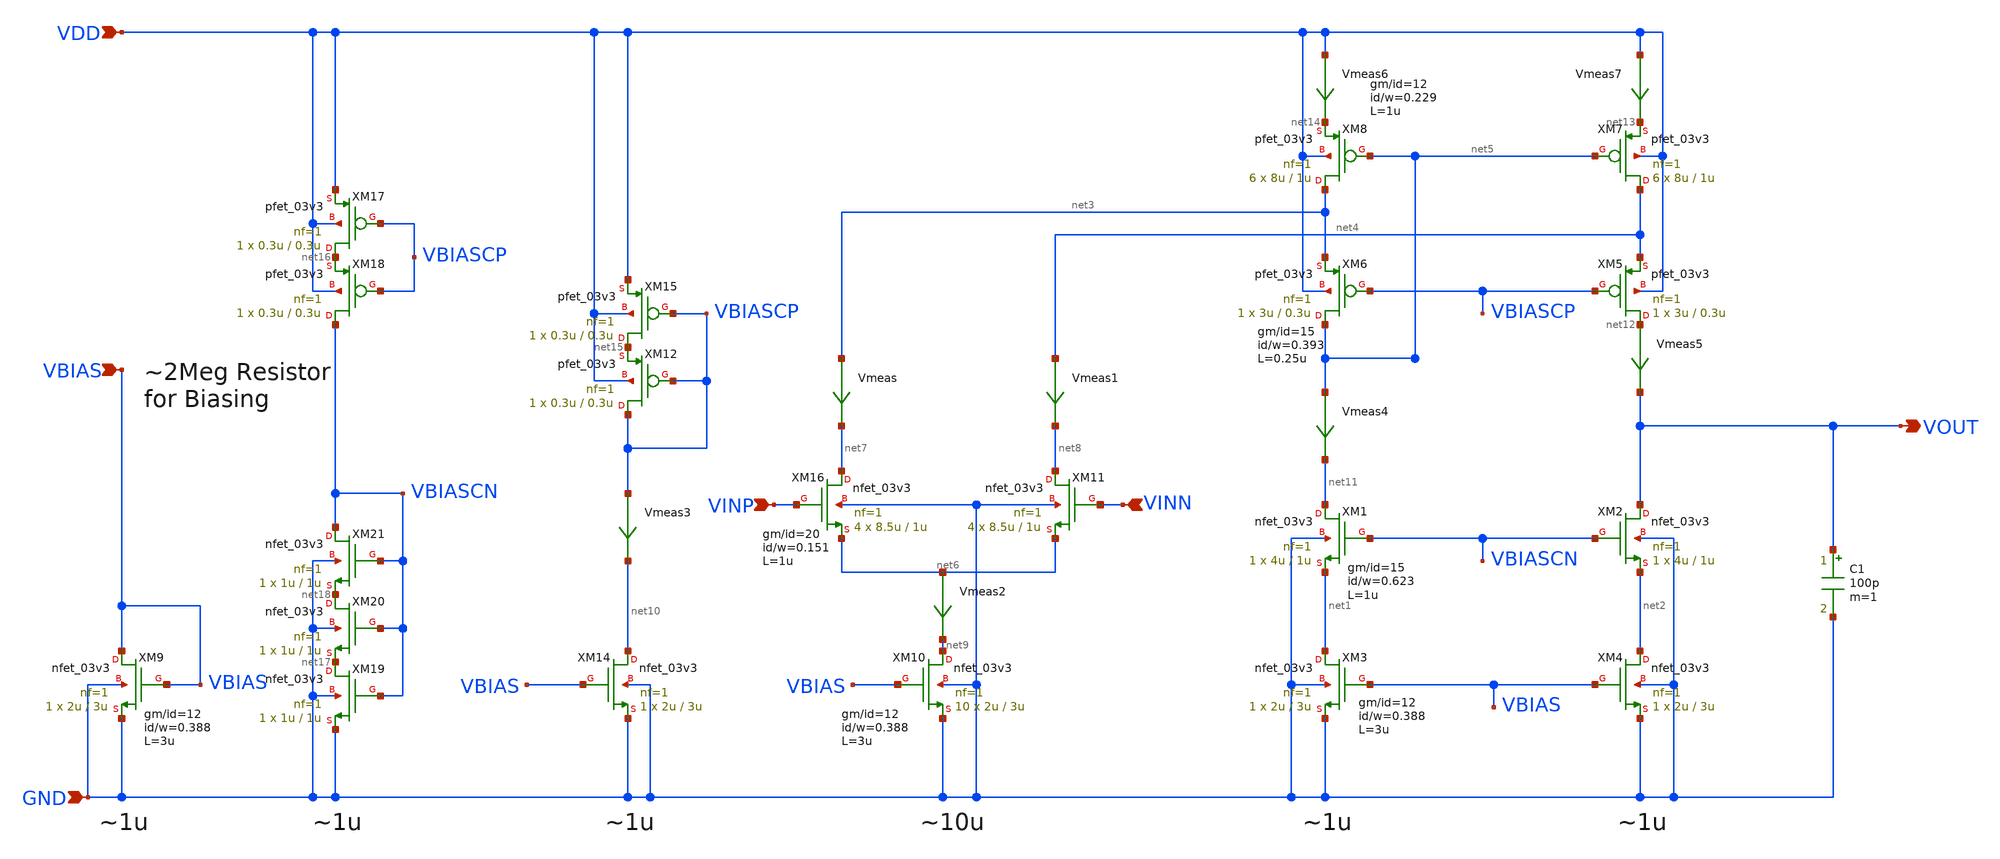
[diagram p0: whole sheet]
** sch_path: SCH/XSCHEM/TTGF0P3_LPCAS_FC_OTA.sch
**.subckt TTGF0P3_LPCAS_FC_OTA VOUT VINP VINN VDD VBIAS GND
*.opin VOUT
*.ipin VINP
*.ipin VINN
*.ipin VDD
*.ipin VBIAS
*.ipin GND
XM1 net11 VBIASCN net1 GND nfet_03v3 L=1u W=4u nf=1 ad='int((nf+1)/2) * W/nf * 0.18u' as='int((nf+2)/2) * W/nf * 0.18u'
+ pd='2*int((nf+1)/2) * (W/nf + 0.18u)' ps='2*int((nf+2)/2) * (W/nf + 0.18u)' nrd='0.18u / W' nrs='0.18u / W'
+ sa=0 sb=0 sd=0 m=1
XM2 VOUT VBIASCN net2 GND nfet_03v3 L=1u W=4u nf=1 ad='int((nf+1)/2) * W/nf * 0.18u' as='int((nf+2)/2) * W/nf * 0.18u'
+ pd='2*int((nf+1)/2) * (W/nf + 0.18u)' ps='2*int((nf+2)/2) * (W/nf + 0.18u)' nrd='0.18u / W' nrs='0.18u / W'
+ sa=0 sb=0 sd=0 m=1
XM5 net12 VBIASCP net4 VDD pfet_03v3 L=0.3u W=3u nf=1 ad='int((nf+1)/2) * W/nf * 0.18u' as='int((nf+2)/2) * W/nf * 0.18u'
+ pd='2*int((nf+1)/2) * (W/nf + 0.18u)' ps='2*int((nf+2)/2) * (W/nf + 0.18u)' nrd='0.18u / W' nrs='0.18u / W'
+ sa=0 sb=0 sd=0 m=1
XM6 net5 VBIASCP net3 VDD pfet_03v3 L=0.3u W=3u nf=1 ad='int((nf+1)/2) * W/nf * 0.18u' as='int((nf+2)/2) * W/nf * 0.18u'
+ pd='2*int((nf+1)/2) * (W/nf + 0.18u)' ps='2*int((nf+2)/2) * (W/nf + 0.18u)' nrd='0.18u / W' nrs='0.18u / W'
+ sa=0 sb=0 sd=0 m=1
XM7 net4 net5 net13 VDD pfet_03v3 L=1u W=8u nf=1 ad='int((nf+1)/2) * W/nf * 0.18u' as='int((nf+2)/2) * W/nf * 0.18u'
+ pd='2*int((nf+1)/2) * (W/nf + 0.18u)' ps='2*int((nf+2)/2) * (W/nf + 0.18u)' nrd='0.18u / W' nrs='0.18u / W'
+ sa=0 sb=0 sd=0 m=6
XM8 net3 net5 net14 VDD pfet_03v3 L=1u W=8u nf=1 ad='int((nf+1)/2) * W/nf * 0.18u' as='int((nf+2)/2) * W/nf * 0.18u'
+ pd='2*int((nf+1)/2) * (W/nf + 0.18u)' ps='2*int((nf+2)/2) * (W/nf + 0.18u)' nrd='0.18u / W' nrs='0.18u / W'
+ sa=0 sb=0 sd=0 m=6
XM9 VBIAS VBIAS GND GND nfet_03v3 L=3u W=2u nf=1 ad='int((nf+1)/2) * W/nf * 0.18u' as='int((nf+2)/2) * W/nf * 0.18u'
+ pd='2*int((nf+1)/2) * (W/nf + 0.18u)' ps='2*int((nf+2)/2) * (W/nf + 0.18u)' nrd='0.18u / W' nrs='0.18u / W'
+ sa=0 sb=0 sd=0 m=1
XM10 net9 VBIAS GND GND nfet_03v3 L=3u W=2u nf=1 ad='int((nf+1)/2) * W/nf * 0.18u' as='int((nf+2)/2) * W/nf * 0.18u'
+ pd='2*int((nf+1)/2) * (W/nf + 0.18u)' ps='2*int((nf+2)/2) * (W/nf + 0.18u)' nrd='0.18u / W' nrs='0.18u / W'
+ sa=0 sb=0 sd=0 m=10
XM3 net1 VBIAS GND GND nfet_03v3 L=3u W=2u nf=1 ad='int((nf+1)/2) * W/nf * 0.18u' as='int((nf+2)/2) * W/nf * 0.18u'
+ pd='2*int((nf+1)/2) * (W/nf + 0.18u)' ps='2*int((nf+2)/2) * (W/nf + 0.18u)' nrd='0.18u / W' nrs='0.18u / W'
+ sa=0 sb=0 sd=0 m=1
XM4 net2 VBIAS GND GND nfet_03v3 L=3u W=2u nf=1 ad='int((nf+1)/2) * W/nf * 0.18u' as='int((nf+2)/2) * W/nf * 0.18u'
+ pd='2*int((nf+1)/2) * (W/nf + 0.18u)' ps='2*int((nf+2)/2) * (W/nf + 0.18u)' nrd='0.18u / W' nrs='0.18u / W'
+ sa=0 sb=0 sd=0 m=1
XM14 net10 VBIAS GND GND nfet_03v3 L=3u W=2u nf=1 ad='int((nf+1)/2) * W/nf * 0.18u' as='int((nf+2)/2) * W/nf * 0.18u'
+ pd='2*int((nf+1)/2) * (W/nf + 0.18u)' ps='2*int((nf+2)/2) * (W/nf + 0.18u)' nrd='0.18u / W' nrs='0.18u / W'
+ sa=0 sb=0 sd=0 m=1
XM15 net15 VBIASCP VDD VDD pfet_03v3 L=0.3u W=0.3u nf=1 ad='int((nf+1)/2) * W/nf * 0.18u' as='int((nf+2)/2) * W/nf * 0.18u'
+ pd='2*int((nf+1)/2) * (W/nf + 0.18u)' ps='2*int((nf+2)/2) * (W/nf + 0.18u)' nrd='0.18u / W' nrs='0.18u / W'
+ sa=0 sb=0 sd=0 m=1
Vmeas net3 net7 0
.save i(vmeas)
Vmeas1 net4 net8 0
.save i(vmeas1)
Vmeas2 net6 net9 0
.save i(vmeas2)
Vmeas3 VBIASCP net10 0
.save i(vmeas3)
Vmeas4 net5 net11 0
.save i(vmeas4)
Vmeas5 net12 VOUT 0
.save i(vmeas5)
XM16 net7 VINP net6 GND nfet_03v3 L=1u W=8.5u nf=1 ad='int((nf+1)/2) * W/nf * 0.18u' as='int((nf+2)/2) * W/nf * 0.18u'
+ pd='2*int((nf+1)/2) * (W/nf + 0.18u)' ps='2*int((nf+2)/2) * (W/nf + 0.18u)' nrd='0.18u / W' nrs='0.18u / W'
+ sa=0 sb=0 sd=0 m=4
XM11 net8 VINN net6 GND nfet_03v3 L=1u W=8.5u nf=1 ad='int((nf+1)/2) * W/nf * 0.18u' as='int((nf+2)/2) * W/nf * 0.18u'
+ pd='2*int((nf+1)/2) * (W/nf + 0.18u)' ps='2*int((nf+2)/2) * (W/nf + 0.18u)' nrd='0.18u / W' nrs='0.18u / W'
+ sa=0 sb=0 sd=0 m=4
Vmeas6 VDD net14 0
.save i(vmeas6)
Vmeas7 VDD net13 0
.save i(vmeas7)
C1 VOUT GND 100p m=1
XM12 VBIASCP VBIASCP net15 VDD pfet_03v3 L=0.3u W=0.3u nf=1 ad='int((nf+1)/2) * W/nf * 0.18u' as='int((nf+2)/2) * W/nf * 0.18u'
+ pd='2*int((nf+1)/2) * (W/nf + 0.18u)' ps='2*int((nf+2)/2) * (W/nf + 0.18u)' nrd='0.18u / W' nrs='0.18u / W'
+ sa=0 sb=0 sd=0 m=1
XM17 net16 VBIASCP VDD VDD pfet_03v3 L=0.3u W=0.3u nf=1 ad='int((nf+1)/2) * W/nf * 0.18u' as='int((nf+2)/2) * W/nf * 0.18u'
+ pd='2*int((nf+1)/2) * (W/nf + 0.18u)' ps='2*int((nf+2)/2) * (W/nf + 0.18u)' nrd='0.18u / W' nrs='0.18u / W'
+ sa=0 sb=0 sd=0 m=1
XM18 VBIASCN VBIASCP net16 VDD pfet_03v3 L=0.3u W=0.3u nf=1 ad='int((nf+1)/2) * W/nf * 0.18u' as='int((nf+2)/2) * W/nf * 0.18u'
+ pd='2*int((nf+1)/2) * (W/nf + 0.18u)' ps='2*int((nf+2)/2) * (W/nf + 0.18u)' nrd='0.18u / W' nrs='0.18u / W'
+ sa=0 sb=0 sd=0 m=1
XM19 net17 VBIASCN GND GND nfet_03v3 L=1u W=1u nf=1 ad='int((nf+1)/2) * W/nf * 0.18u' as='int((nf+2)/2) * W/nf * 0.18u'
+ pd='2*int((nf+1)/2) * (W/nf + 0.18u)' ps='2*int((nf+2)/2) * (W/nf + 0.18u)' nrd='0.18u / W' nrs='0.18u / W'
+ sa=0 sb=0 sd=0 m=1
XM20 net18 VBIASCN net17 GND nfet_03v3 L=1u W=1u nf=1 ad='int((nf+1)/2) * W/nf * 0.18u' as='int((nf+2)/2) * W/nf * 0.18u'
+ pd='2*int((nf+1)/2) * (W/nf + 0.18u)' ps='2*int((nf+2)/2) * (W/nf + 0.18u)' nrd='0.18u / W' nrs='0.18u / W'
+ sa=0 sb=0 sd=0 m=1
XM21 VBIASCN VBIASCN net18 GND nfet_03v3 L=1u W=1u nf=1 ad='int((nf+1)/2) * W/nf * 0.18u' as='int((nf+2)/2) * W/nf * 0.18u'
+ pd='2*int((nf+1)/2) * (W/nf + 0.18u)' ps='2*int((nf+2)/2) * (W/nf + 0.18u)' nrd='0.18u / W' nrs='0.18u / W'
+ sa=0 sb=0 sd=0 m=1
**.ends
.end
